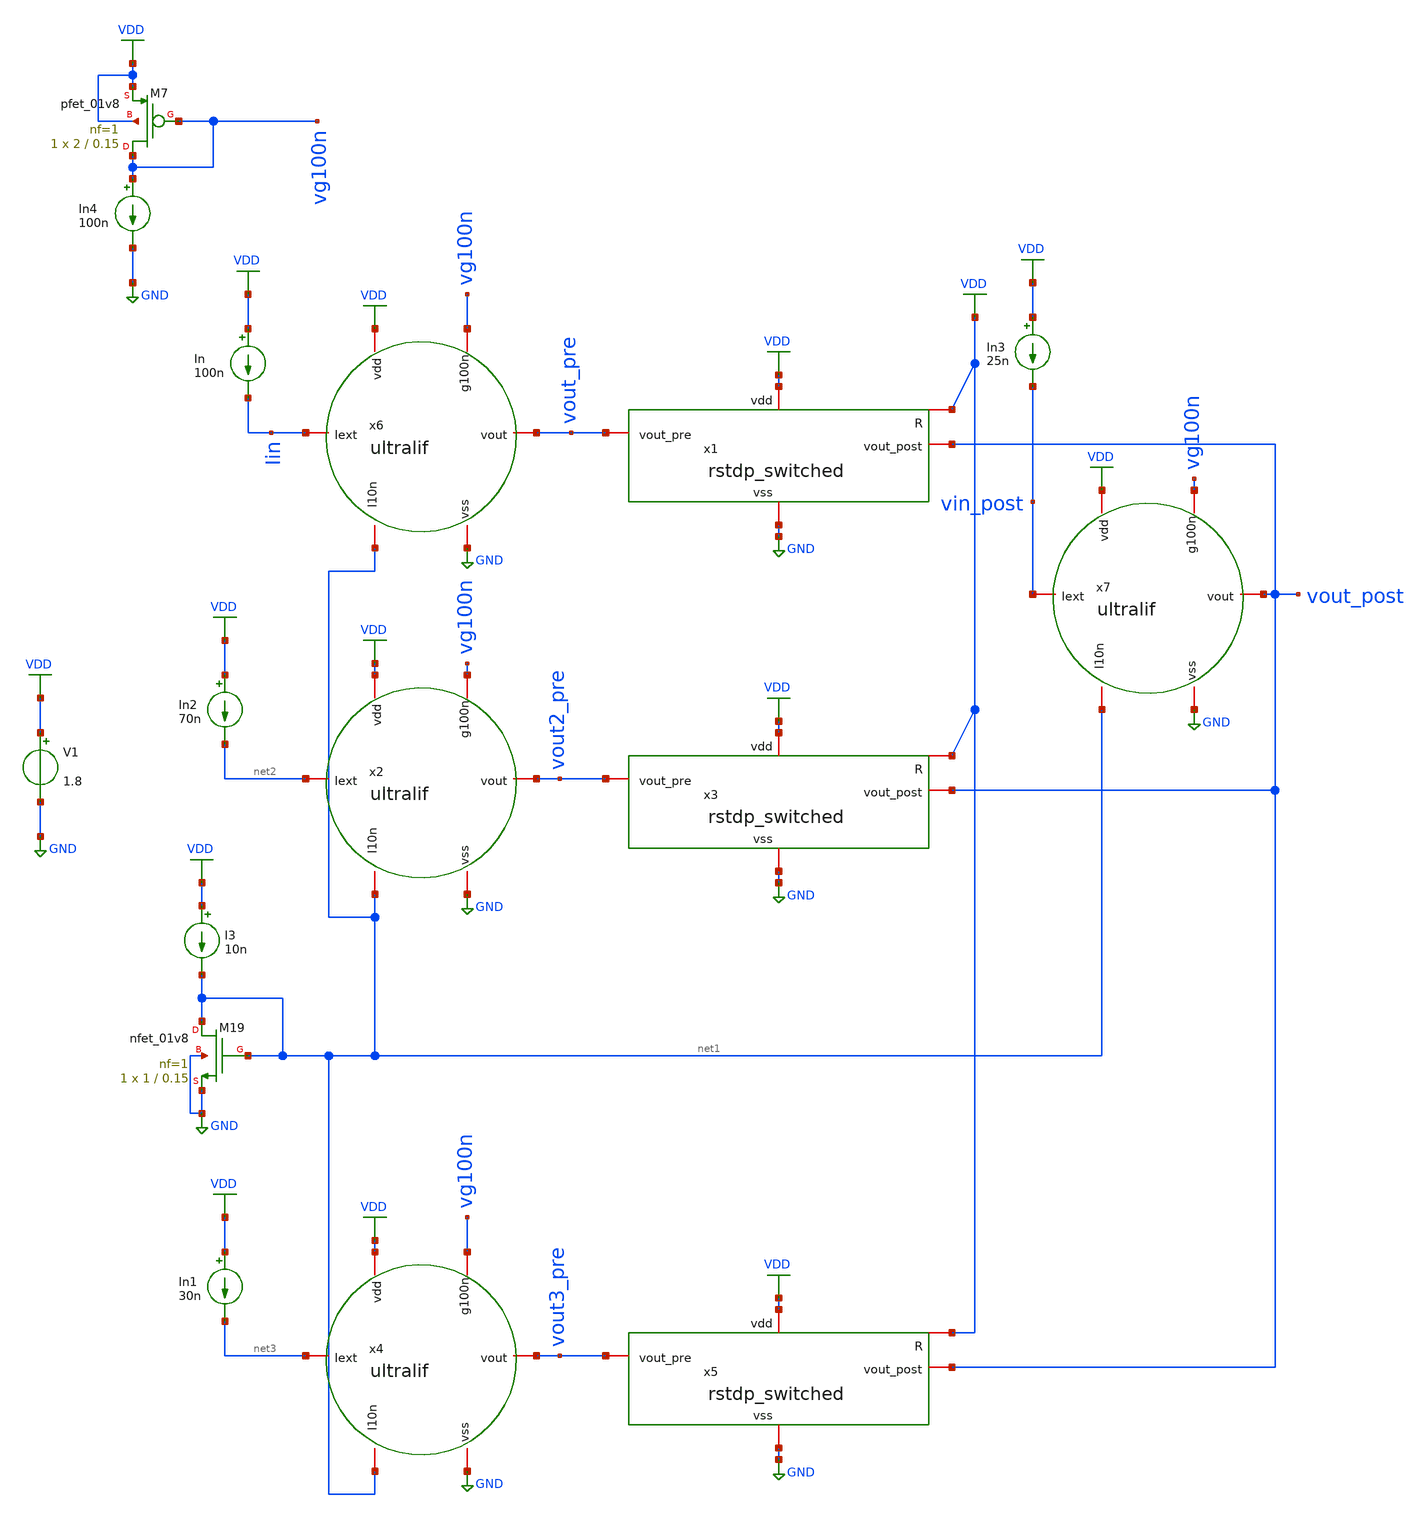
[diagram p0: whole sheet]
** sch_path: tb_1_1.sch
**.subckt tb_1_1
V1 VDD GND 1.8
x6 VDD Iin vout_pre net1 GND vg100n ultralif
x7 VDD vin_post vout_post net1 GND vg100n ultralif
XM19 net1 net1 GND GND sky130_fd_pr__nfet_01v8 L=0.15 W=1 nf=1 ad='int((nf+1)/2) * W/nf * 0.29' as='int((nf+2)/2) * W/nf * 0.29'
+ pd='2*int((nf+1)/2) * (W/nf + 0.29)' ps='2*int((nf+2)/2) * (W/nf + 0.29)' nrd='0.29 / W' nrs='0.29 / W'
+ sa=0 sb=0 sd=0 mult=1 m=1
I3 VDD net1 10n
x1 VDD VDD GND vout_pre vout_post rstdp_switched
In VDD Iin 100n
x2 VDD net2 vout2_pre net1 GND vg100n ultralif
In2 VDD net2 70n
x3 VDD VDD GND vout2_pre vout_post rstdp_switched
x4 VDD net3 vout3_pre net1 GND vg100n ultralif
In1 VDD net3 30n
x5 VDD VDD GND vout3_pre vout_post rstdp_switched
In3 VDD vin_post 25n
XM7 vg100n vg100n VDD VDD sky130_fd_pr__pfet_01v8 L=0.15 W=2 nf=1 ad='int((nf+1)/2) * W/nf * 0.29' as='int((nf+2)/2) * W/nf * 0.29'
+ pd='2*int((nf+1)/2) * (W/nf + 0.29)' ps='2*int((nf+2)/2) * (W/nf + 0.29)' nrd='0.29 / W' nrs='0.29 / W'
+ sa=0 sb=0 sd=0 mult=1 m=1
In4 vg100n GND 100n
**** begin user architecture code
.lib $::SKYWATER_MODELS/sky130.lib.spice tt

** opencircuitdesign pdks install
.inc $::SKYWATER_MODELS/rram_v0.spice

**** end user architecture code
**.ends

* expanding   symbol:  /home/alex/Desktop/EDA/SNN_IPN/Neuron/ultralif/ultralif.sym # of pins=6
** sym_path: Neuron/ultralif/ultralif.sym
** sch_path: Neuron/ultralif/ultralif.sch
.subckt ultralif vdd Iext vout I10n vss g100n
*.iopin Iext
*.iopin vout
*.iopin vss
*.iopin I10n
*.iopin vdd
*.iopin g100n
XM1 net2 net2 vm vdd sky130_fd_pr__pfet_01v8 L=10 W=1 nf=1 ad='int((nf+1)/2) * W/nf * 0.29' as='int((nf+2)/2) * W/nf * 0.29'
+ pd='2*int((nf+1)/2) * (W/nf + 0.29)' ps='2*int((nf+2)/2) * (W/nf + 0.29)' nrd='0.29 / W' nrs='0.29 / W'
+ sa=0 sb=0 sd=0 mult=1 m=1
XM2 net2 net1 vm vdd sky130_fd_pr__pfet_01v8 L=0.15 W=1.5 nf=1 ad='int((nf+1)/2) * W/nf * 0.29' as='int((nf+2)/2) * W/nf * 0.29'
+ pd='2*int((nf+1)/2) * (W/nf + 0.29)' ps='2*int((nf+2)/2) * (W/nf + 0.29)' nrd='0.29 / W' nrs='0.29 / W'
+ sa=0 sb=0 sd=0 mult=1 m=1
XM3 net1 net1 vm vdd sky130_fd_pr__pfet_01v8 L=0.15 W=5 nf=1 ad='int((nf+1)/2) * W/nf * 0.29' as='int((nf+2)/2) * W/nf * 0.29'
+ pd='2*int((nf+1)/2) * (W/nf + 0.29)' ps='2*int((nf+2)/2) * (W/nf + 0.29)' nrd='0.29 / W' nrs='0.29 / W'
+ sa=0 sb=0 sd=0 mult=2 m=2
XM4 net1 net2 vss vss sky130_fd_pr__nfet_01v8 L=4 W=1 nf=1 ad='int((1 + 1)/2) * 1 / 1 * 0.29' as='int((1 + 2)/2) * 1 / 1 * 0.29'
+ pd='2*int((1 + 1)/2) * (1 / 1 + 0.29)' ps='2*int((1 + 2)/2) * (1 / 1 + 0.29)' nrd='0.29 / 1 ' nrs='0.29 / 1 '
+ sa=0 sb=0 sd=0 mult=1 m=1
C1 vm vss 0.1p m=1
XM9 vm net2 net3 vdd sky130_fd_pr__pfet_01v8 L=0.15 W=2 nf=1 ad='int((nf+1)/2) * W/nf * 0.29' as='int((nf+2)/2) * W/nf * 0.29'
+ pd='2*int((nf+1)/2) * (W/nf + 0.29)' ps='2*int((nf+2)/2) * (W/nf + 0.29)' nrd='0.29 / W' nrs='0.29 / W'
+ sa=0 sb=0 sd=0 mult=1 m=1
XM10 net2 I10n vss vss sky130_fd_pr__nfet_01v8 L=0.15 W=1 nf=1 ad='int((1 + 1)/2) * 1 / 1 * 0.29' as='int((1 + 2)/2) * 1 / 1 * 0.29'
+ pd='2*int((1 + 1)/2) * (1 / 1 + 0.29)' ps='2*int((1 + 2)/2) * (1 / 1 + 0.29)' nrd='0.29 / 1 ' nrs='0.29 / 1 '
+ sa=0 sb=0 sd=0 mult=1 m=1
XM5 net4 net2 vss vss sky130_fd_pr__nfet_01v8 L=0.15 W=1 nf=1 ad='int((1 + 1)/2) * 1 / 1 * 0.29' as='int((1 + 2)/2) * 1 / 1 * 0.29'
+ pd='2*int((1 + 1)/2) * (1 / 1 + 0.29)' ps='2*int((1 + 2)/2) * (1 / 1 + 0.29)' nrd='0.29 / 1 ' nrs='0.29 / 1 '
+ sa=0 sb=0 sd=0 mult=1 m=1
XM6 net4 g100n vdd vdd sky130_fd_pr__pfet_01v8 L=0.15 W=2 nf=1 ad='int((nf+1)/2) * W/nf * 0.29' as='int((nf+2)/2) * W/nf * 0.29'
+ pd='2*int((nf+1)/2) * (W/nf + 0.29)' ps='2*int((nf+2)/2) * (W/nf + 0.29)' nrd='0.29 / W' nrs='0.29 / W'
+ sa=0 sb=0 sd=0 mult=1 m=1
XM7 vout net4 vss vss sky130_fd_pr__nfet_01v8 L=0.15 W=1 nf=1 ad='int((1 + 1)/2) * 1 / 1 * 0.29' as='int((1 + 2)/2) * 1 / 1 * 0.29'
+ pd='2*int((1 + 1)/2) * (1 / 1 + 0.29)' ps='2*int((1 + 2)/2) * (1 / 1 + 0.29)' nrd='0.29 / 1 ' nrs='0.29 / 1 '
+ sa=0 sb=0 sd=0 mult=1 m=1
XM11 vout net4 vdd vdd sky130_fd_pr__pfet_01v8 L=0.15 W=2 nf=1 ad='int((nf+1)/2) * W/nf * 0.29' as='int((nf+2)/2) * W/nf * 0.29'
+ pd='2*int((nf+1)/2) * (W/nf + 0.29)' ps='2*int((nf+2)/2) * (W/nf + 0.29)' nrd='0.29 / W' nrs='0.29 / W'
+ sa=0 sb=0 sd=0 mult=1 m=1
XM8 Iext Iext net3 vss sky130_fd_pr__nfet_01v8 L=0.15 W=1 nf=1 ad='int((1 + 1)/2) * 1 / 1 * 0.29' as='int((1 + 2)/2) * 1 / 1 * 0.29'
+ pd='2*int((1 + 1)/2) * (1 / 1 + 0.29)' ps='2*int((1 + 2)/2) * (1 / 1 + 0.29)' nrd='0.29 / 1 ' nrs='0.29 / 1 '
+ sa=0 sb=0 sd=0 mult=1 m=1
.ends


* expanding   symbol:  /home/alex/Desktop/EDA/SNN_IPN/Synapse/rstdp_switched.sym # of pins=5
** sym_path: Synapse/rstdp_switched.sym
** sch_path: Synapse/rstdp_switched.sch
.subckt rstdp_switched vdd R vss vout_pre vout_post
*.iopin vdd
*.iopin vss
*.iopin R
*.iopin vout_post
*.iopin vout_pre
XR2 te be rram_v0
XM2 vpre R be vss sky130_fd_pr__nfet_01v8 L=0.15 W=7.5 nf=1 ad='int((nf+1)/2) * W/nf * 0.29' as='int((nf+2)/2) * W/nf * 0.29'
+ pd='2*int((nf+1)/2) * (W/nf + 0.29)' ps='2*int((nf+2)/2) * (W/nf + 0.29)' nrd='0.29 / W' nrs='0.29 / W'
+ sa=0 sb=0 sd=0 mult=1 m=1
XM3 te R vpost vss sky130_fd_pr__nfet_01v8 L=0.15 W=7.5 nf=1 ad='int((nf+1)/2) * W/nf * 0.29' as='int((nf+2)/2) * W/nf * 0.29'
+ pd='2*int((nf+1)/2) * (W/nf + 0.29)' ps='2*int((nf+2)/2) * (W/nf + 0.29)' nrd='0.29 / W' nrs='0.29 / W'
+ sa=0 sb=0 sd=0 mult=1 m=1
XM1 te R vpre vdd sky130_fd_pr__pfet_01v8 L=0.15 W=15 nf=1 ad='int((nf+1)/2) * W/nf * 0.29' as='int((nf+2)/2) * W/nf * 0.29'
+ pd='2*int((nf+1)/2) * (W/nf + 0.29)' ps='2*int((nf+2)/2) * (W/nf + 0.29)' nrd='0.29 / W' nrs='0.29 / W'
+ sa=0 sb=0 sd=0 mult=2 m=2
XM4 vpost R be vdd sky130_fd_pr__pfet_01v8 L=0.15 W=15 nf=1 ad='int((nf+1)/2) * W/nf * 0.29' as='int((nf+2)/2) * W/nf * 0.29'
+ pd='2*int((nf+1)/2) * (W/nf + 0.29)' ps='2*int((nf+2)/2) * (W/nf + 0.29)' nrd='0.29 / W' nrs='0.29 / W'
+ sa=0 sb=0 sd=0 mult=2 m=2
XM7 vpost vout_post vss vss sky130_fd_pr__nfet_01v8 L=0.15 W=1 nf=1 ad='int((1 + 1)/2) * 1 / 1 * 0.29'
+ as='int((1 + 2)/2) * 1 / 1 * 0.29' pd='2*int((1 + 1)/2) * (1 / 1 + 0.29)' ps='2*int((1 + 2)/2) * (1 / 1 + 0.29)'
+ nrd='0.29 / 1 ' nrs='0.29 / 1 ' sa=0 sb=0 sd=0 mult=1 m=1
XM5 vpost vout_post vdd vdd sky130_fd_pr__pfet_01v8 L=0.15 W=2 nf=1 ad='int((nf+1)/2) * W/nf * 0.29'
+ as='int((nf+2)/2) * W/nf * 0.29' pd='2*int((nf+1)/2) * (W/nf + 0.29)' ps='2*int((nf+2)/2) * (W/nf + 0.29)'
+ nrd='0.29 / W' nrs='0.29 / W' sa=0 sb=0 sd=0 mult=1 m=1
XM6 vpre vout_pre vss vss sky130_fd_pr__nfet_01v8 L=0.15 W=1 nf=1 ad='int((1 + 1)/2) * 1 / 1 * 0.29'
+ as='int((1 + 2)/2) * 1 / 1 * 0.29' pd='2*int((1 + 1)/2) * (1 / 1 + 0.29)' ps='2*int((1 + 2)/2) * (1 / 1 + 0.29)'
+ nrd='0.29 / 1 ' nrs='0.29 / 1 ' sa=0 sb=0 sd=0 mult=1 m=1
XM8 vpre vout_pre vdd vdd sky130_fd_pr__pfet_01v8 L=0.15 W=2 nf=1 ad='int((nf+1)/2) * W/nf * 0.29' as='int((nf+2)/2) * W/nf * 0.29'
+ pd='2*int((nf+1)/2) * (W/nf + 0.29)' ps='2*int((nf+2)/2) * (W/nf + 0.29)' nrd='0.29 / W' nrs='0.29 / W'
+ sa=0 sb=0 sd=0 mult=1 m=1
.ends

.GLOBAL VDD
.GLOBAL GND
**** begin user architecture code


*.options savecurrents
.tran 100n 100u uic
.control
	run
	write tb_1_1.raw
.endc


**** end user architecture code
.end
